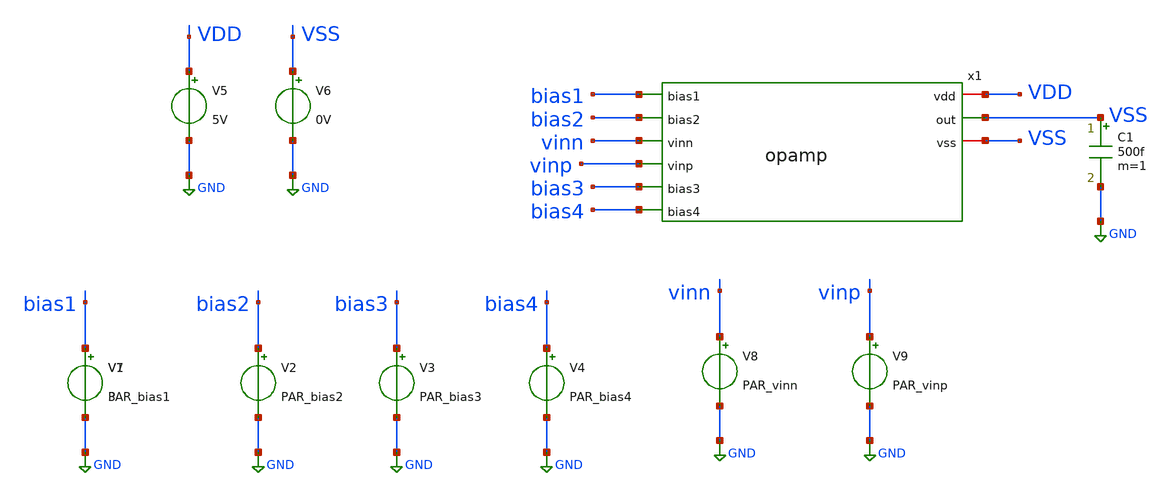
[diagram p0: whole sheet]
** sch_path: activities/opamp2AKAM/testBenchOpamp.sch
**.subckt testBenchOpamp
V1 bias1 GND PAR_bias1
V2 bias2 GND PAR_bias2
V3 bias3 GND PAR_bias3
V4 bias4 GND PAR_bias4
V5 VDD GND 5V
V6 VSS GND 0V
V7 bias1 GND 3
x1 VDD bias1 bias2 vinn VSS vinp bias3 bias4 VSS opamp
V8 vinn GND PAR_vinn
V9 vinp GND PAR_vinp
C1 VSS GND 500f m=1
**.ends
.GLOBAL GND
.end
